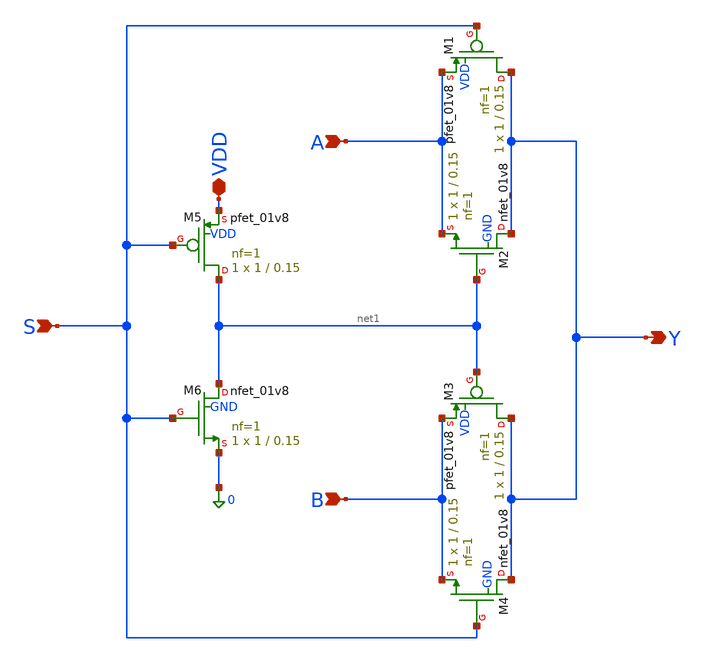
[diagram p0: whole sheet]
** sch_path: schematic/mux21.sch
**.subckt mux21 A B S Y VDD
*.ipin A
*.ipin B
*.ipin S
*.opin Y
*.iopin VDD
XM1 Y S A VDD sky130_fd_pr__pfet_01v8 L=0.15 W=1 nf=1 ad='int((1 + 1)/2) * 1 / 1 * 0.29' as='int((1 + 2)/2) * 1 / 1 * 0.29'
+ pd='2*int((1 + 1)/2) * (1 / 1 + 0.29)' ps='2*int((1 + 2)/2) * (1 / 1 + 0.29)' nrd='0.29 / 1 ' nrs='0.29 / 1 '
+ sa=0 sb=0 sd=0 mult=1 m=1
XM2 Y net1 A GND sky130_fd_pr__nfet_01v8 L=0.15 W=1 nf=1 ad='int((1 + 1)/2) * 1 / 1 * 0.29' as='int((1 + 2)/2) * 1 / 1 * 0.29'
+ pd='2*int((1 + 1)/2) * (1 / 1 + 0.29)' ps='2*int((1 + 2)/2) * (1 / 1 + 0.29)' nrd='0.29 / 1 ' nrs='0.29 / 1 '
+ sa=0 sb=0 sd=0 mult=1 m=1
XM3 Y net1 B VDD sky130_fd_pr__pfet_01v8 L=0.15 W=1 nf=1 ad='int((1 + 1)/2) * 1 / 1 * 0.29' as='int((1 + 2)/2) * 1 / 1 * 0.29'
+ pd='2*int((1 + 1)/2) * (1 / 1 + 0.29)' ps='2*int((1 + 2)/2) * (1 / 1 + 0.29)' nrd='0.29 / 1 ' nrs='0.29 / 1 '
+ sa=0 sb=0 sd=0 mult=1 m=1
XM4 Y S B GND sky130_fd_pr__nfet_01v8 L=0.15 W=1 nf=1 ad='int((1 + 1)/2) * 1 / 1 * 0.29' as='int((1 + 2)/2) * 1 / 1 * 0.29'
+ pd='2*int((1 + 1)/2) * (1 / 1 + 0.29)' ps='2*int((1 + 2)/2) * (1 / 1 + 0.29)' nrd='0.29 / 1 ' nrs='0.29 / 1 '
+ sa=0 sb=0 sd=0 mult=1 m=1
XM5 net1 S VDD VDD sky130_fd_pr__pfet_01v8 L=0.15 W=1 nf=1 ad='int((1 + 1)/2) * 1 / 1 * 0.29' as='int((1 + 2)/2) * 1 / 1 * 0.29'
+ pd='2*int((1 + 1)/2) * (1 / 1 + 0.29)' ps='2*int((1 + 2)/2) * (1 / 1 + 0.29)' nrd='0.29 / 1 ' nrs='0.29 / 1 '
+ sa=0 sb=0 sd=0 mult=1 m=1
XM6 net1 S 0 GND sky130_fd_pr__nfet_01v8 L=0.15 W=1 nf=1 ad='int((1 + 1)/2) * 1 / 1 * 0.29' as='int((1 + 2)/2) * 1 / 1 * 0.29'
+ pd='2*int((1 + 1)/2) * (1 / 1 + 0.29)' ps='2*int((1 + 2)/2) * (1 / 1 + 0.29)' nrd='0.29 / 1 ' nrs='0.29 / 1 '
+ sa=0 sb=0 sd=0 mult=1 m=1
**.ends
.end
